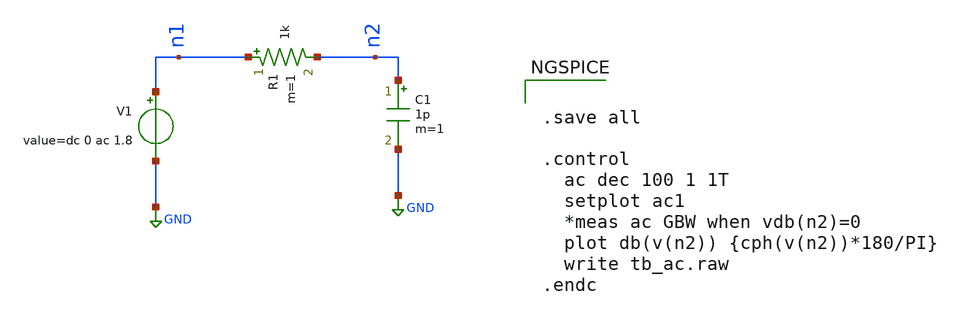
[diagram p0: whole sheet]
** sch_path: Synapse/tb_ac.sch
**.subckt tb_ac
V1 n1 GND dc 0 ac 1.8
R1 n1 n2 1k m=1
C1 n2 GND 1p m=1
**** begin user architecture code


.save all

.control
  ac dec 100 1 1T
  setplot ac1
  *meas ac GBW when vdb(n2)=0
  plot db(v(n2)) {cph(v(n2))*180/PI}
  write tb_ac.raw
.endc



**** end user architecture code
**.ends
.GLOBAL GND
.end
